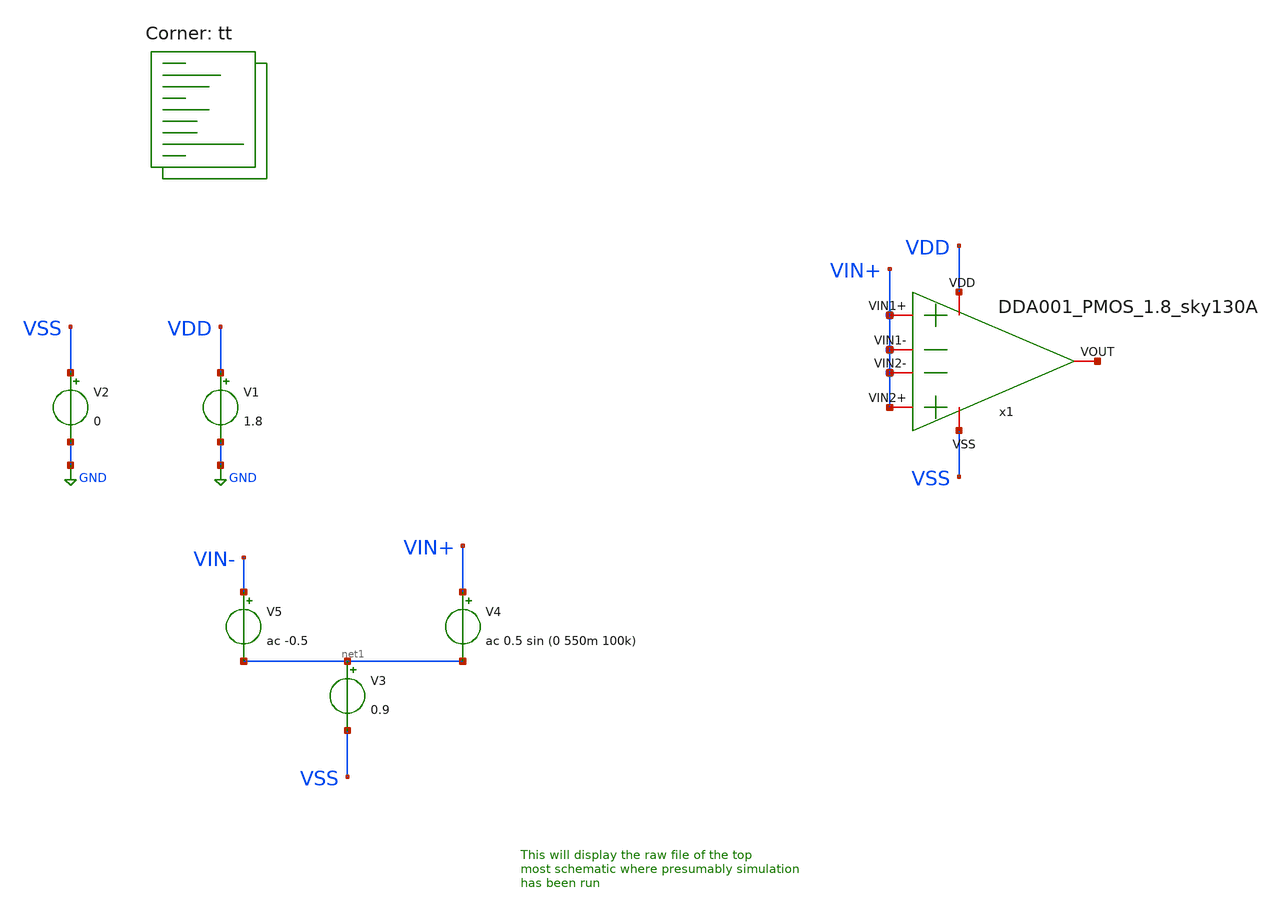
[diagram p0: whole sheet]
** sch_path: my_ip/sky130A/DDA_testbenches/op_tb.sch
**.subckt op_tb
V1 VDD GND 1.8
V2 VSS GND 0
V3 net1 VSS 0.9
V4 VIN+ net1 ac 0.5 sin (0 550m 100k)
V5 VIN- net1 ac -0.5
x1 VDD VSS VIN+ VIN+ net2 VIN+ VIN+ DDA001_PMOS_1.8_sky130A
**** begin user architecture code
.lib $::SKYWATER_MODELS/sky130.lib.spice tt
**** end user architecture code
**.ends

* expanding   symbol:  DDA001_PMOS_1.8_sky130A .sym # of pins=7
** sym_path: LIB/Sky130A/DDA/DDA001_PMOS_1.8_sky130A .sym
** sch_path: LIB/Sky130A/DDA/DDA001_PMOS_1.8_sky130A .sch
.subckt DDA001_PMOS_1.8_sky130A  VDD VSS VIN1- VIN1+ VOUT VIN2- VIN2+
*.iopin VDD
*.iopin VSS
*.iopin VIN1-
*.iopin VIN1+
*.iopin VOUT
*.iopin VIN2-
*.iopin VIN2+
XM1 VB1 VB1 VDD VDD sky130_fd_pr__pfet_01v8_lvt L=1 W='3 * 4 ' nf=4 ad='int((4 + 1)/2) * 3 / 4 * 0.29'
+ as='int((4 + 2)/2) * 3 / 4 * 0.29' pd='2*int((4 + 1)/2) * (3 / 4 + 0.29)' ps='2*int((4 + 2)/2) * (3 / 4 + 0.29)'
+ nrd='0.29 / 3 ' nrs='0.29 / 3 ' sa=0 sb=0 sd=0 mult=2 m=2
XM2 VCFsdsd VB1 VDD VDD sky130_fd_pr__pfet_01v8_lvt L=1 W='3 * 4 ' nf=4 ad='int((4 + 1)/2) * 3 / 4 * 0.29'
+ as='int((4 + 2)/2) * 3 / 4 * 0.29' pd='2*int((4 + 1)/2) * (3 / 4 + 0.29)' ps='2*int((4 + 2)/2) * (3 / 4 + 0.29)'
+ nrd='0.29 / 3 ' nrs='0.29 / 3 ' sa=0 sb=0 sd=0 mult=16 m=16
XM3 net1 VB1 VDD VDD sky130_fd_pr__pfet_01v8_lvt L=1 W='3 * 4 ' nf=4 ad='int((4 + 1)/2) * 3 / 4 * 0.29'
+ as='int((4 + 2)/2) * 3 / 4 * 0.29' pd='2*int((4 + 1)/2) * (3 / 4 + 0.29)' ps='2*int((4 + 2)/2) * (3 / 4 + 0.29)'
+ nrd='0.29 / 3 ' nrs='0.29 / 3 ' sa=0 sb=0 sd=0 mult=16 m=16
XM4 VCF VIN1- VCFsdsd VDD sky130_fd_pr__pfet_01v8_lvt L=2 W='4 * 4 ' nf=4 ad='int((4 + 1)/2) * 4 / 4 * 0.29'
+ as='int((4 + 2)/2) * 4 / 4 * 0.29' pd='2*int((4 + 1)/2) * (4 / 4 + 0.29)' ps='2*int((4 + 2)/2) * (4 / 4 + 0.29)'
+ nrd='0.29 / 4 ' nrs='0.29 / 4 ' sa=0 sb=0 sd=0 mult=4 m=4
XM8 VCF VCF VSS VSS sky130_fd_pr__nfet_01v8 L=2 W='1 * 4 ' nf=4 ad='int((4 + 1)/2) * 1 / 4 * 0.29' as='int((4 + 2)/2) * 1 / 4 * 0.29'
+ pd='2*int((4 + 1)/2) * (1 / 4 + 0.29)' ps='2*int((4 + 2)/2) * (1 / 4 + 0.29)' nrd='0.29 / 1 ' nrs='0.29 / 1 '
+ sa=0 sb=0 sd=0 mult=2 m=2
XM9 VC VCF VSS VSS sky130_fd_pr__nfet_01v8 L=2 W='1 * 4 ' nf=4 ad='int((4 + 1)/2) * 1 / 4 * 0.29' as='int((4 + 2)/2) * 1 / 4 * 0.29'
+ pd='2*int((4 + 1)/2) * (1 / 4 + 0.29)' ps='2*int((4 + 2)/2) * (1 / 4 + 0.29)' nrd='0.29 / 1 ' nrs='0.29 / 1 '
+ sa=0 sb=0 sd=0 mult=2 m=2
XM10 VCFff VCFff VSS VSS sky130_fd_pr__nfet_01v8 L=2 W='1 * 4 ' nf=4 ad='int((4 + 1)/2) * 1 / 4 * 0.29'
+ as='int((4 + 2)/2) * 1 / 4 * 0.29' pd='2*int((4 + 1)/2) * (1 / 4 + 0.29)' ps='2*int((4 + 2)/2) * (1 / 4 + 0.29)'
+ nrd='0.29 / 1 ' nrs='0.29 / 1 ' sa=0 sb=0 sd=0 mult=2 m=2
XM11 VOUT VCFff VSS VSS sky130_fd_pr__nfet_01v8 L=2 W='1 * 4 ' nf=4 ad='int((4 + 1)/2) * 1 / 4 * 0.29'
+ as='int((4 + 2)/2) * 1 / 4 * 0.29' pd='2*int((4 + 1)/2) * (1 / 4 + 0.29)' ps='2*int((4 + 2)/2) * (1 / 4 + 0.29)'
+ nrd='0.29 / 1 ' nrs='0.29 / 1 ' sa=0 sb=0 sd=0 mult=2 m=2
XM12 VC VC VDD VDD sky130_fd_pr__pfet_01v8 L=1 W='4 * 4 ' nf=4 ad= as='int((4 + 2)/2) * 4 * 0.29' pd='2*int((4 + 1)/2) * (4 + 0.29)'
+ ps='2*int((4 + 2)/2) * (4 + 0.29)' nrd='0.29 / 4 / 4 ' nrs='0.29 / 4 / 4 ' sa=0 sb=0 sd=0 mult=2 m=2
XM13 VOUT VC VDD VDD sky130_fd_pr__pfet_01v8 L=1 W='4 * 4 ' nf=4 ad= as='int((4 + 2)/2) * 4 * 0.29' pd='2*int((4 + 1)/2) * (4 + 0.29)'
+ ps='2*int((4 + 2)/2) * (4 + 0.29)' nrd='0.29 / 4 / 4 ' nrs='0.29 / 4 / 4 ' sa=0 sb=0 sd=0 mult=2 m=2
XM5 VCF VIN2- net1 VDD sky130_fd_pr__pfet_01v8_lvt L=2 W='4 * 4 ' nf=4 ad='int((4 + 1)/2) * 4 / 4 * 0.29'
+ as='int((4 + 2)/2) * 4 / 4 * 0.29' pd='2*int((4 + 1)/2) * (4 / 4 + 0.29)' ps='2*int((4 + 2)/2) * (4 / 4 + 0.29)'
+ nrd='0.29 / 4 ' nrs='0.29 / 4 ' sa=0 sb=0 sd=0 mult=4 m=4
XM6 VCFff VIN1+ VCFsdsd VDD sky130_fd_pr__pfet_01v8_lvt L=2 W='4 * 4 ' nf=4 ad='int((4 + 1)/2) * 4 / 4 * 0.29'
+ as='int((4 + 2)/2) * 4 / 4 * 0.29' pd='2*int((4 + 1)/2) * (4 / 4 + 0.29)' ps='2*int((4 + 2)/2) * (4 / 4 + 0.29)'
+ nrd='0.29 / 4 ' nrs='0.29 / 4 ' sa=0 sb=0 sd=0 mult=4 m=4
XM7 VCFff VIN2+ net1 VDD sky130_fd_pr__pfet_01v8_lvt L=2 W='4 * 4 ' nf=4 ad='int((4 + 1)/2) * 4 / 4 * 0.29'
+ as='int((4 + 2)/2) * 4 / 4 * 0.29' pd='2*int((4 + 1)/2) * (4 / 4 + 0.29)' ps='2*int((4 + 2)/2) * (4 / 4 + 0.29)'
+ nrd='0.29 / 4 ' nrs='0.29 / 4 ' sa=0 sb=0 sd=0 mult=4 m=4
XR10 VSS net6 VSS sky130_fd_pr__res_xhigh_po_0p35 L=0.4 mult=2 m=2
XM14 net2 net3 net5 VSS sky130_fd_pr__nfet_01v8 L=3 W='2 * 2 ' nf=2 ad='int((2 + 1)/2) * 2 / 2 * 0.29'
+ as='int((2 + 2)/2) * 2 / 2 * 0.29' pd='2*int((2 + 1)/2) * (2 / 2 + 0.29)' ps='2*int((2 + 2)/2) * (2 / 2 + 0.29)'
+ nrd='0.29 / 2 ' nrs='0.29 / 2 ' sa=0 sb=0 sd=0 mult=4 m=4
XM15 net3 net3 net4 VSS sky130_fd_pr__nfet_01v8 L=3 W='2 * 2 ' nf=2 ad='int((2 + 1)/2) * 2 / 2 * 0.29'
+ as='int((2 + 2)/2) * 2 / 2 * 0.29' pd='2*int((2 + 1)/2) * (2 / 2 + 0.29)' ps='2*int((2 + 2)/2) * (2 / 2 + 0.29)'
+ nrd='0.29 / 2 ' nrs='0.29 / 2 ' sa=0 sb=0 sd=0 mult=4 m=4
XM16 net5 net4 net6 VSS sky130_fd_pr__nfet_01v8 L=2 W='3 * 2 ' nf=2 ad='int((2 + 1)/2) * 3 / 2 * 0.29'
+ as='int((2 + 2)/2) * 3 / 2 * 0.29' pd='2*int((2 + 1)/2) * (3 / 2 + 0.29)' ps='2*int((2 + 2)/2) * (3 / 2 + 0.29)'
+ nrd='0.29 / 3 ' nrs='0.29 / 3 ' sa=0 sb=0 sd=0 mult=8 m=8
XM17 net4 net4 VSS VSS sky130_fd_pr__nfet_01v8 L=2 W='3 * 2 ' nf=2 ad='int((2 + 1)/2) * 3 / 2 * 0.29'
+ as='int((2 + 2)/2) * 3 / 2 * 0.29' pd='2*int((2 + 1)/2) * (3 / 2 + 0.29)' ps='2*int((2 + 2)/2) * (3 / 2 + 0.29)'
+ nrd='0.29 / 3 ' nrs='0.29 / 3 ' sa=0 sb=0 sd=0 mult=2 m=2
XM18 net3 net2 VDD VDD sky130_fd_pr__pfet_01v8_lvt L=3 W='4 * 2 ' nf=2 ad='int((2 + 1)/2) * 4 / 2 * 0.29'
+ as='int((2 + 2)/2) * 4 / 2 * 0.29' pd='2*int((2 + 1)/2) * (4 / 2 + 0.29)' ps='2*int((2 + 2)/2) * (4 / 2 + 0.29)'
+ nrd='0.29 / 4 ' nrs='0.29 / 4 ' sa=0 sb=0 sd=0 mult=2 m=2
XM19 net2 net2 VDD VDD sky130_fd_pr__pfet_01v8_lvt L=3 W='4 * 2 ' nf=2 ad='int((2 + 1)/2) * 4 / 2 * 0.29'
+ as='int((2 + 2)/2) * 4 / 2 * 0.29' pd='2*int((2 + 1)/2) * (4 / 2 + 0.29)' ps='2*int((2 + 2)/2) * (4 / 2 + 0.29)'
+ nrd='0.29 / 4 ' nrs='0.29 / 4 ' sa=0 sb=0 sd=0 mult=2 m=2
XM20 VB1 net4 VSS VSS sky130_fd_pr__nfet_01v8 L=2 W='3 * 2 ' nf=2 ad='int((2 + 1)/2) * 3 / 2 * 0.29'
+ as='int((2 + 2)/2) * 3 / 2 * 0.29' pd='2*int((2 + 1)/2) * (3 / 2 + 0.29)' ps='2*int((2 + 2)/2) * (3 / 2 + 0.29)'
+ nrd='0.29 / 3 ' nrs='0.29 / 3 ' sa=0 sb=0 sd=0 mult=2 m=2
.ends

.GLOBAL GND
**** begin user architecture code


* ngspice commands
.options savecurrents
.TEMP 27
.control
save all
save @m.x1.xm1.msky130_fd_pr__pfet_01v8_lvt[gm]
save @m.x1.xm1.msky130_fd_pr__pfet_01v8_lvt[vth]
save @m.x1.xm1.msky130_fd_pr__pfet_01v8_lvt[gds]
save @m.x1.xm1.msky130_fd_pr__pfet_01v8_lvt[gmbs]
save @m.x1.xm1.msky130_fd_pr__pfet_01v8_lvt[vds]
save @m.x1.xm1.msky130_fd_pr__pfet_01v8_lvt[vgs]


save @m.x1.xm2.msky130_fd_pr__pfet_01v8_lvt[gm]
save @m.x1.xm2.msky130_fd_pr__pfet_01v8_lvt[vth]
save @m.x1.xm2.msky130_fd_pr__pfet_01v8_lvt[gds]
save @m.x1.xm2.msky130_fd_pr__pfet_01v8_lvt[gmbs]
save @m.x1.xm2.msky130_fd_pr__pfet_01v8_lvt[vds]
save @m.x1.xm2.msky130_fd_pr__pfet_01v8_lvt[vgs]

save @m.x1.xm3.msky130_fd_pr__nfet_01v8[gm]
save @m.x1.xm3.msky130_fd_pr__nfet_01v8[vth]
save @m.x1.xm3.msky130_fd_pr__nfet_01v8[gds]
save @m.x1.xm3.msky130_fd_pr__nfet_01v8[gmbs]
save @m.x1.xm3.msky130_fd_pr__nfet_01v8[vds]
save @m.x1.xm3.msky130_fd_pr__nfet_01v8[vgs]

save @m.x1.xm4.msky130_fd_pr__nfet_01v8[gm]
save @m.x1.xm4.msky130_fd_pr__nfet_01v8[vth]
save @m.x1.xm4.msky130_fd_pr__nfet_01v8[gds]
save @m.x1.xm4.msky130_fd_pr__nfet_01v8[gmbs]
save @m.x1.xm4.msky130_fd_pr__nfet_01v8[vds]
save @m.x1.xm4.msky130_fd_pr__nfet_01v8[vgs]

save @m.x1.xm5.msky130_fd_pr__nfet_01v8[gm]
save @m.x1.xm5.msky130_fd_pr__nfet_01v8[vth]
save @m.x1.xm5.msky130_fd_pr__nfet_01v8[gds]
save @m.x1.xm5.msky130_fd_pr__nfet_01v8[gmbs]
save @m.x1.xm5.msky130_fd_pr__nfet_01v8[vds]
save @m.x1.xm5.msky130_fd_pr__nfet_01v8[vgs]

save @m.x1.xm6.msky130_fd_pr__nfet_01v8[gm]
save @m.x1.xm6.msky130_fd_pr__nfet_01v8[vth]
save @m.x1.xm6.msky130_fd_pr__nfet_01v8[gds]
save @m.x1.xm6.msky130_fd_pr__nfet_01v8[gmbs]
save @m.x1.xm6.msky130_fd_pr__nfet_01v8[vds]
save @m.x1.xm6.msky130_fd_pr__nfet_01v8[vgs]

save @m.x1.xm7.msky130_fd_pr__pfet_01v8_lvt[gm]
save @m.x1.xm7.msky130_fd_pr__pfet_01v8_lvt[vth]
save @m.x1.xm7.msky130_fd_pr__pfet_01v8_lvt[gds]
save @m.x1.xm7.msky130_fd_pr__pfet_01v8_lvt[gmbs]
save @m.x1.xm7.msky130_fd_pr__pfet_01v8_lvt[vds]
save @m.x1.xm7.msky130_fd_pr__pfet_01v8_lvt[vgs]

save @m.x1.xm8.msky130_fd_pr__pfet_01v8_lvt[gm]
save @m.x1.xm8.msky130_fd_pr__pfet_01v8_lvt[vth]
save @m.x1.xm8.msky130_fd_pr__pfet_01v8_lvt[gds]
save @m.x1.xm8.msky130_fd_pr__pfet_01v8_lvt[gmbs]
save @m.x1.xm8.msky130_fd_pr__pfet_01v8_lvt[vds]
save @m.x1.xm8.msky130_fd_pr__pfet_01v8_lvt[vgs]

save @m.x1.xm9.msky130_fd_pr__pfet_01v8_lvt[gm]
save @m.x1.xm9.msky130_fd_pr__pfet_01v8_lvt[vth]
save @m.x1.xm9.msky130_fd_pr__pfet_01v8_lvt[gds]
save @m.x1.xm9.msky130_fd_pr__pfet_01v8_lvt[gmbs]
save @m.x1.xm9.msky130_fd_pr__pfet_01v8_lvt[vds]
save @m.x1.xm9.msky130_fd_pr__pfet_01v8_lvt[vgs]


save @m.x1.xm10.msky130_fd_pr__nfet_01v8[gm]
save @m.x1.xm10.msky130_fd_pr__nfet_01v8[vth]
save @m.x1.xm10.msky130_fd_pr__nfet_01v8[gds]
save @m.x1.xm10.msky130_fd_pr__nfet_01v8[gmbs]
save @m.x1.xm10.msky130_fd_pr__nfet_01v8[vds]
save @m.x1.xm10.msky130_fd_pr__nfet_01v8[vgs]


save @m.x1.xm11.msky130_fd_pr__nfet_01v8[gm]
save @m.x1.xm11.msky130_fd_pr__nfet_01v8[vth]
save @m.x1.xm11.msky130_fd_pr__nfet_01v8[gds]
save @m.x1.xm11.msky130_fd_pr__nfet_01v8[gmbs]
save @m.x1.xm11.msky130_fd_pr__nfet_01v8[vds]
save @m.x1.xm11.msky130_fd_pr__nfet_01v8[vgs]

save @m.x1.xm12.msky130_fd_pr__pfet_01v8_lvt[gm]
save @m.x1.xm12.msky130_fd_pr__pfet_01v8_lvt[vth]
save @m.x1.xm12.msky130_fd_pr__pfet_01v8_lvt[gds]
save @m.x1.xm12.msky130_fd_pr__pfet_01v8_lvt[gmbs]
save @m.x1.xm12.msky130_fd_pr__pfet_01v8_lvt[vds]
save @m.x1.xm12.msky130_fd_pr__pfet_01v8_lvt[vgs]

save @m.x1.xm13.msky130_fd_pr__nfet_01v8[gm]
save @m.x1.xm13.msky130_fd_pr__nfet_01v8[vth]
save @m.x1.xm13.msky130_fd_pr__nfet_01v8[gds]
save @m.x1.xm13.msky130_fd_pr__nfet_01v8[gmbs]
save @m.x1.xm13.msky130_fd_pr__nfet_01v8[vds]
save @m.x1.xm13.msky130_fd_pr__nfet_01v8[vgs]




op
write op_tb.raw

.endc



**** end user architecture code
.end
